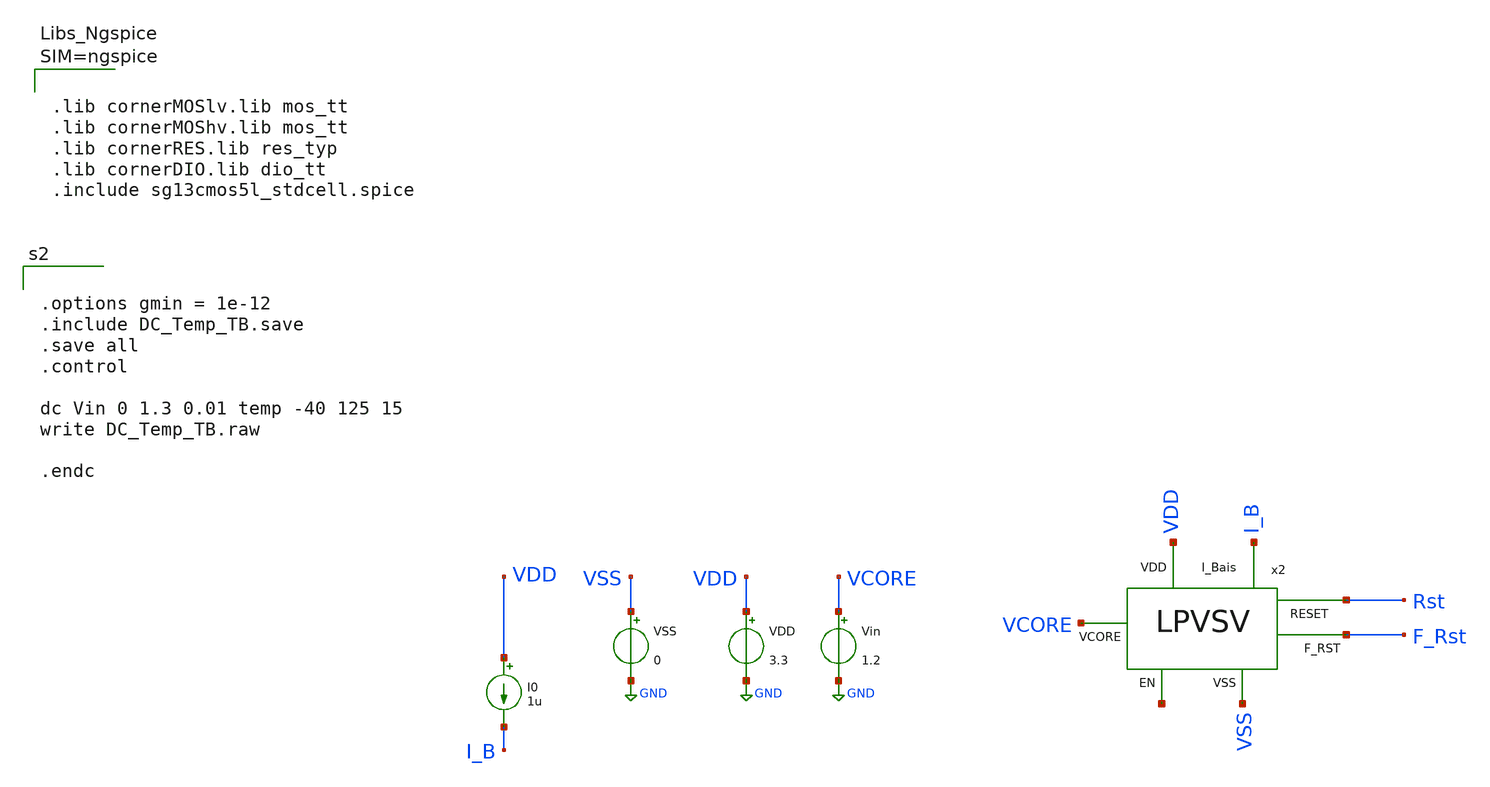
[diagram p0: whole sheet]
** sch_path: Simulation/DC_Temp_TB.sch
**.subckt DC_Temp_TB
VDD VDD GND 3.3
VSS VSS GND 0
Vin VCORE GND 1.2
I0 VDD I_B 1u
x2 VDD VCORE I_B Rst F_Rst VSS net1 LPVSV
**** begin user architecture code


.options gmin = 1e-12
.include DC_Temp_TB.save
.save all
.control

dc Vin 0 1.3 0.01 temp -40 125 15
write DC_Temp_TB.raw

.endc




.options rshunt = 1e15
.options gmin=1e-9
.options reltol = 0.01 abstol = 1p
.option filetype=ascii





.lib cornerMOSlv.lib mos_tt
.lib cornerMOShv.lib mos_tt
.lib cornerRES.lib res_typ
.lib cornerDIO.lib dio_tt
.include sg13cmos5l_stdcell.spice



**** end user architecture code
**.ends
.GLOBAL GND
.end
